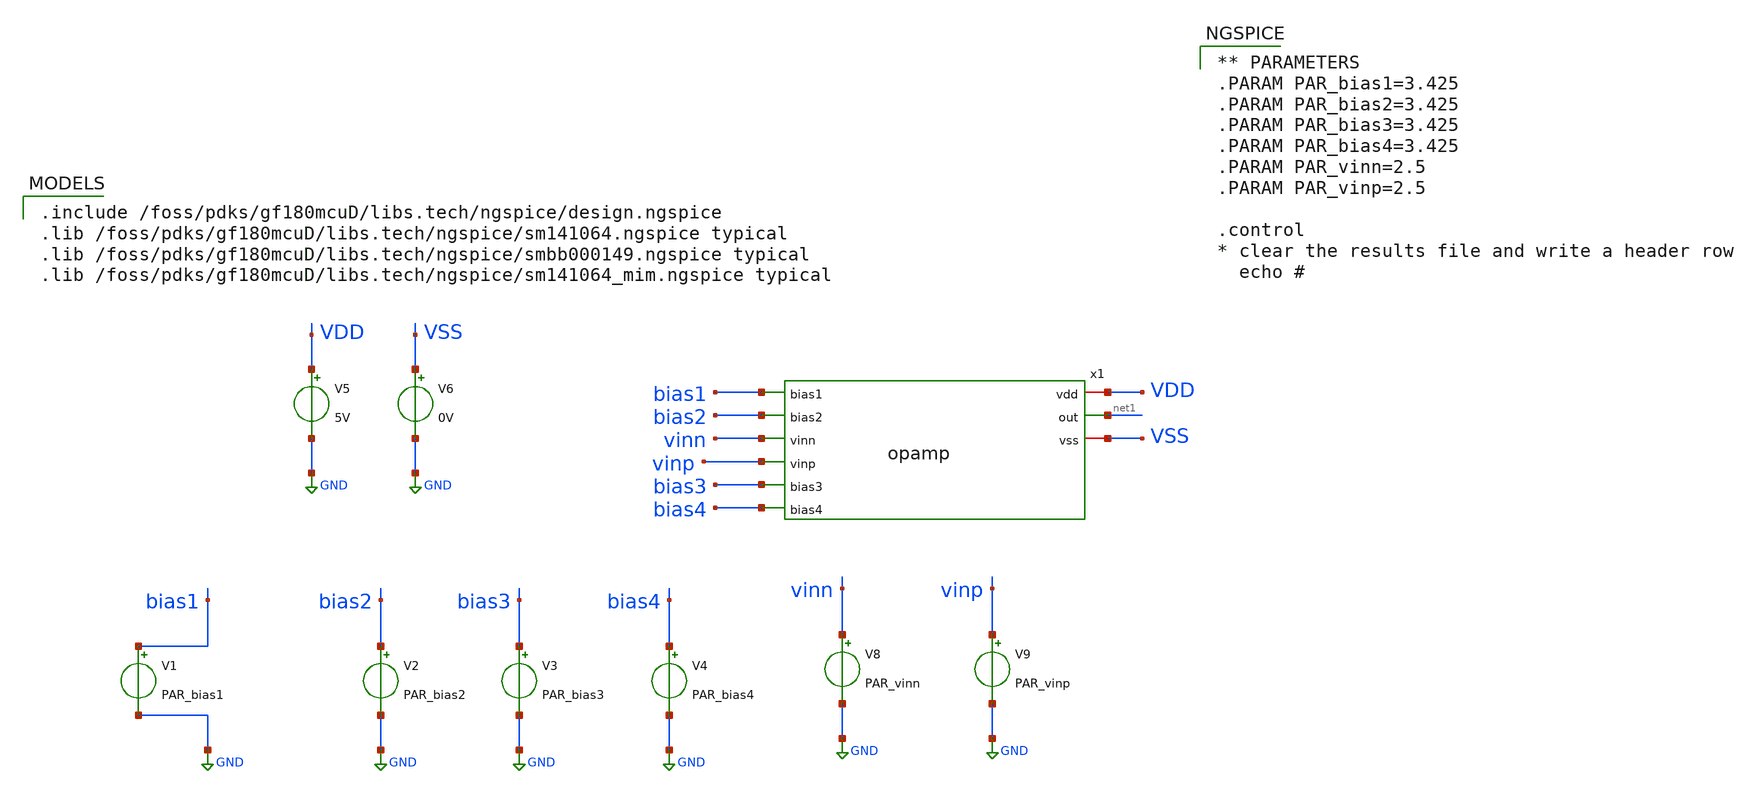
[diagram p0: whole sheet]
** sch_path: activities/opamp2AKAM/testBenchOpamp.sch
**.subckt testBenchOpamp
V1 bias1 GND PAR_bias1
V2 bias2 GND PAR_bias2
V3 bias3 GND PAR_bias3
V4 bias4 GND PAR_bias4
V5 VDD GND 5V
V6 VSS GND 0V
V8 vinn GND PAR_vinn
V9 vinp GND PAR_vinp
x1 VDD bias1 bias2 vinn net1 vinp bias3 bias4 VSS opamp
**** begin user architecture code

.include /foss/pdks/gf180mcuD/libs.tech/ngspice/design.ngspice
.lib /foss/pdks/gf180mcuD/libs.tech/ngspice/sm141064.ngspice typical
.lib /foss/pdks/gf180mcuD/libs.tech/ngspice/smbb000149.ngspice typical
.lib /foss/pdks/gf180mcuD/libs.tech/ngspice/sm141064_mim.ngspice typical


** PARAMETERS
.PARAM PAR_bias1=3.425
.PARAM PAR_bias2=3.425
.PARAM PAR_bias3=3.425
.PARAM PAR_bias4=3.425
.PARAM PAR_vinn=2.5
.PARAM PAR_vinp=2.5

.control
* clear the results file and write a header row
  echo #

**** end user architecture code
**.ends
.GLOBAL GND
.end
